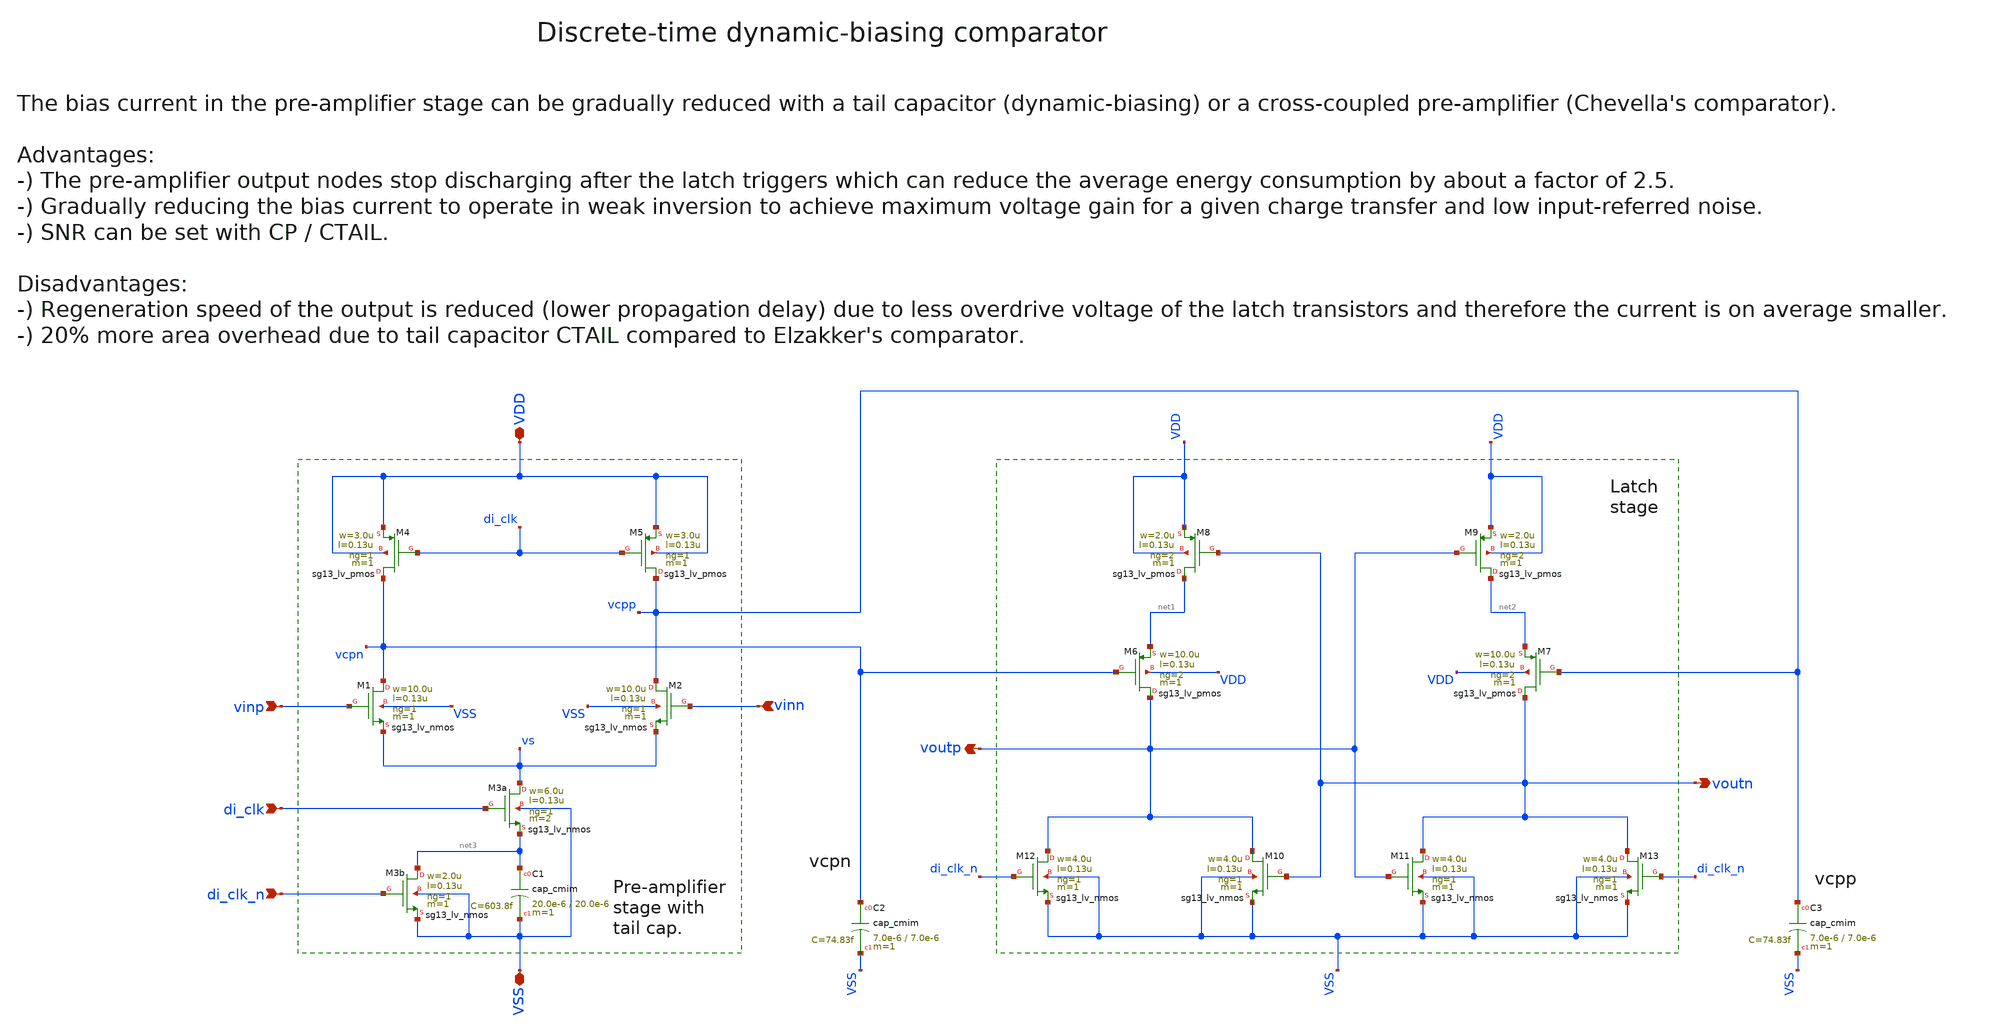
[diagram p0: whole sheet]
** sch_path: xschem/comparator/discrete_time/Dynamic-biasing/dynamic_biasing_comparator.sch
**.subckt dynamic_biasing_comparator VDD voutp voutn di_clk_n VSS vinp vinn di_clk
*.iopin VDD
*.opin voutp
*.opin voutn
*.ipin di_clk_n
*.iopin VSS
*.ipin vinp
*.ipin vinn
*.ipin di_clk
XM3a vs di_clk net3 VSS sg13_lv_nmos w=6.0u l=0.13u ng=1 m=2 mm_ok=1
XM12 voutp di_clk_n VSS VSS sg13_lv_nmos w=4.0u l=0.13u ng=1 m=1 mm_ok=1
XM8 net1 voutn VDD VDD sg13_lv_pmos w=2.0u l=0.13u ng=2 m=1 mm_ok=1
XM10 voutp voutn VSS VSS sg13_lv_nmos w=4.0u l=0.13u ng=1 m=1 mm_ok=1
XM11 voutn voutp VSS VSS sg13_lv_nmos w=4.0u l=0.13u ng=1 m=1 mm_ok=1
XM13 voutn di_clk_n VSS VSS sg13_lv_nmos w=4.0u l=0.13u ng=1 m=1 mm_ok=1
XM9 net2 voutp VDD VDD sg13_lv_pmos w=2.0u l=0.13u ng=2 m=1 mm_ok=1
XM6 voutp vcpn net1 VDD sg13_lv_pmos w=10.0u l=0.13u ng=2 m=1 mm_ok=1
XM7 voutn vcpp net2 VDD sg13_lv_pmos w=10.0u l=0.13u ng=2 m=1 mm_ok=1
XM3b net3 di_clk_n VSS VSS sg13_lv_nmos w=2.0u l=0.13u ng=1 m=1 mm_ok=1
XM1 vcpn vinp vs VSS sg13_lv_nmos w=10.0u l=0.13u ng=1 m=1 mm_ok=1
XM2 vcpp vinn vs VSS sg13_lv_nmos w=10.0u l=0.13u ng=1 m=1 mm_ok=1
XM4 vcpn di_clk VDD VDD sg13_lv_pmos w=3.0u l=0.13u ng=1 m=1 mm_ok=1
XM5 vcpp di_clk VDD VDD sg13_lv_pmos w=3.0u l=0.13u ng=1 m=1 mm_ok=1
XC1 net3 VSS cap_cmim w=20.0e-6 l=20.0e-6 m=1 mm_ok=1
XC2 vcpn VSS cap_cmim w=7.0e-6 l=7.0e-6 m=1 mm_ok=1
XC3 vcpp VSS cap_cmim w=7.0e-6 l=7.0e-6 m=1 mm_ok=1
**.ends
.end
